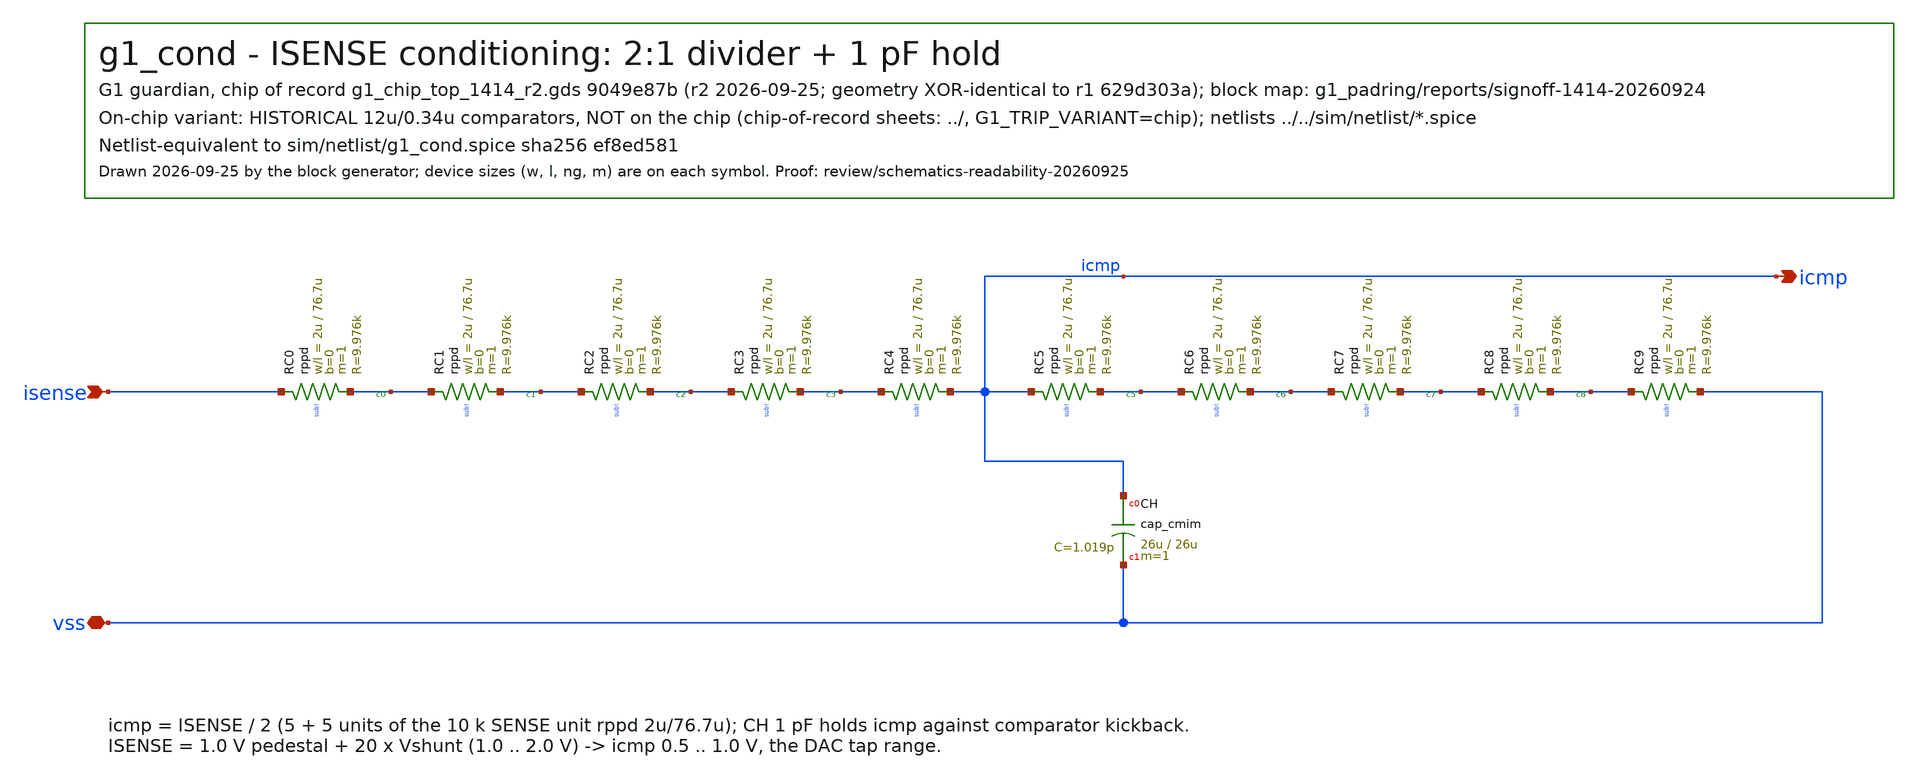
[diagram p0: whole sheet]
** sch_path: designs/g1-guardian/blocks/g1_trip/schematic/historical_12u034/g1_cond.sch
**.subckt g1_cond isense icmp vss
*.ipin isense
*.opin icmp
*.iopin vss
XRC0 isense c0 sub! rppd w=2u l=76.7u m=1 b=0 mm_ok=1
XRC1 c0 c1 sub! rppd w=2u l=76.7u m=1 b=0 mm_ok=1
XRC2 c1 c2 sub! rppd w=2u l=76.7u m=1 b=0 mm_ok=1
XRC3 c2 c3 sub! rppd w=2u l=76.7u m=1 b=0 mm_ok=1
XRC4 c3 icmp sub! rppd w=2u l=76.7u m=1 b=0 mm_ok=1
XRC5 icmp c5 sub! rppd w=2u l=76.7u m=1 b=0 mm_ok=1
XRC6 c5 c6 sub! rppd w=2u l=76.7u m=1 b=0 mm_ok=1
XRC7 c6 c7 sub! rppd w=2u l=76.7u m=1 b=0 mm_ok=1
XRC8 c7 c8 sub! rppd w=2u l=76.7u m=1 b=0 mm_ok=1
XRC9 c8 vss sub! rppd w=2u l=76.7u m=1 b=0 mm_ok=1
XCH icmp vss cap_cmim w=26u l=26u m=1 mm_ok=1
**.ends
.end
